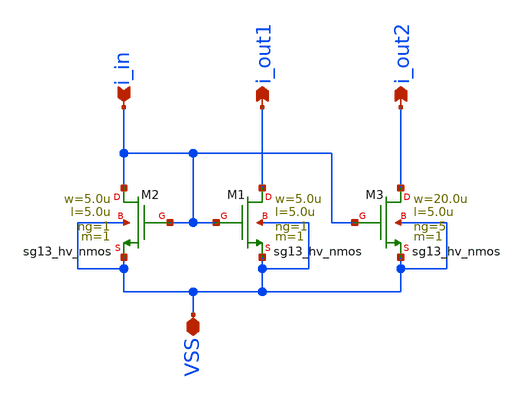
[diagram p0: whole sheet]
** sch_path: macros/heichips26_vcr/macros/switched_capacitor/schematic/xschem/nmos_current_mirror2.sch
**.subckt nmos_current_mirror2 i_in i_out1 VSS i_out2
*.ipin i_in
*.opin i_out1
*.iopin VSS
*.opin i_out2
XM1 i_out1 i_in VSS VSS sg13_hv_nmos w=5.0u l=5.0u ng=1 m=1 mm_ok=1
XM2 i_in i_in VSS VSS sg13_hv_nmos w=5.0u l=5.0u ng=1 m=1 mm_ok=1
XM3 i_out2 i_in VSS VSS sg13_hv_nmos w=20.0u l=5.0u ng=5 m=1 mm_ok=1
**.ends
.end
